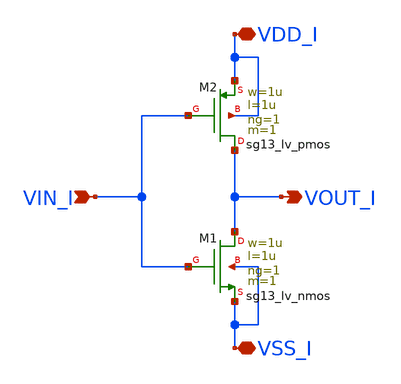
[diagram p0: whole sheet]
** sch_path: xschem/inv/inv.sch
**.subckt inv VDD_I VSS_I VOUT_I VIN_I
*.iopin VDD_I
*.iopin VSS_I
*.opin VOUT_I
*.ipin VIN_I
XM2 VOUT_I VIN_I VDD_I VDD_I sg13_lv_pmos w=1u l=1u ng=1 m=1 mm_ok=1
XM1 VOUT_I VIN_I VSS_I VSS_I sg13_lv_nmos w=1u l=1u ng=1 m=1 mm_ok=1
**.ends
.end
